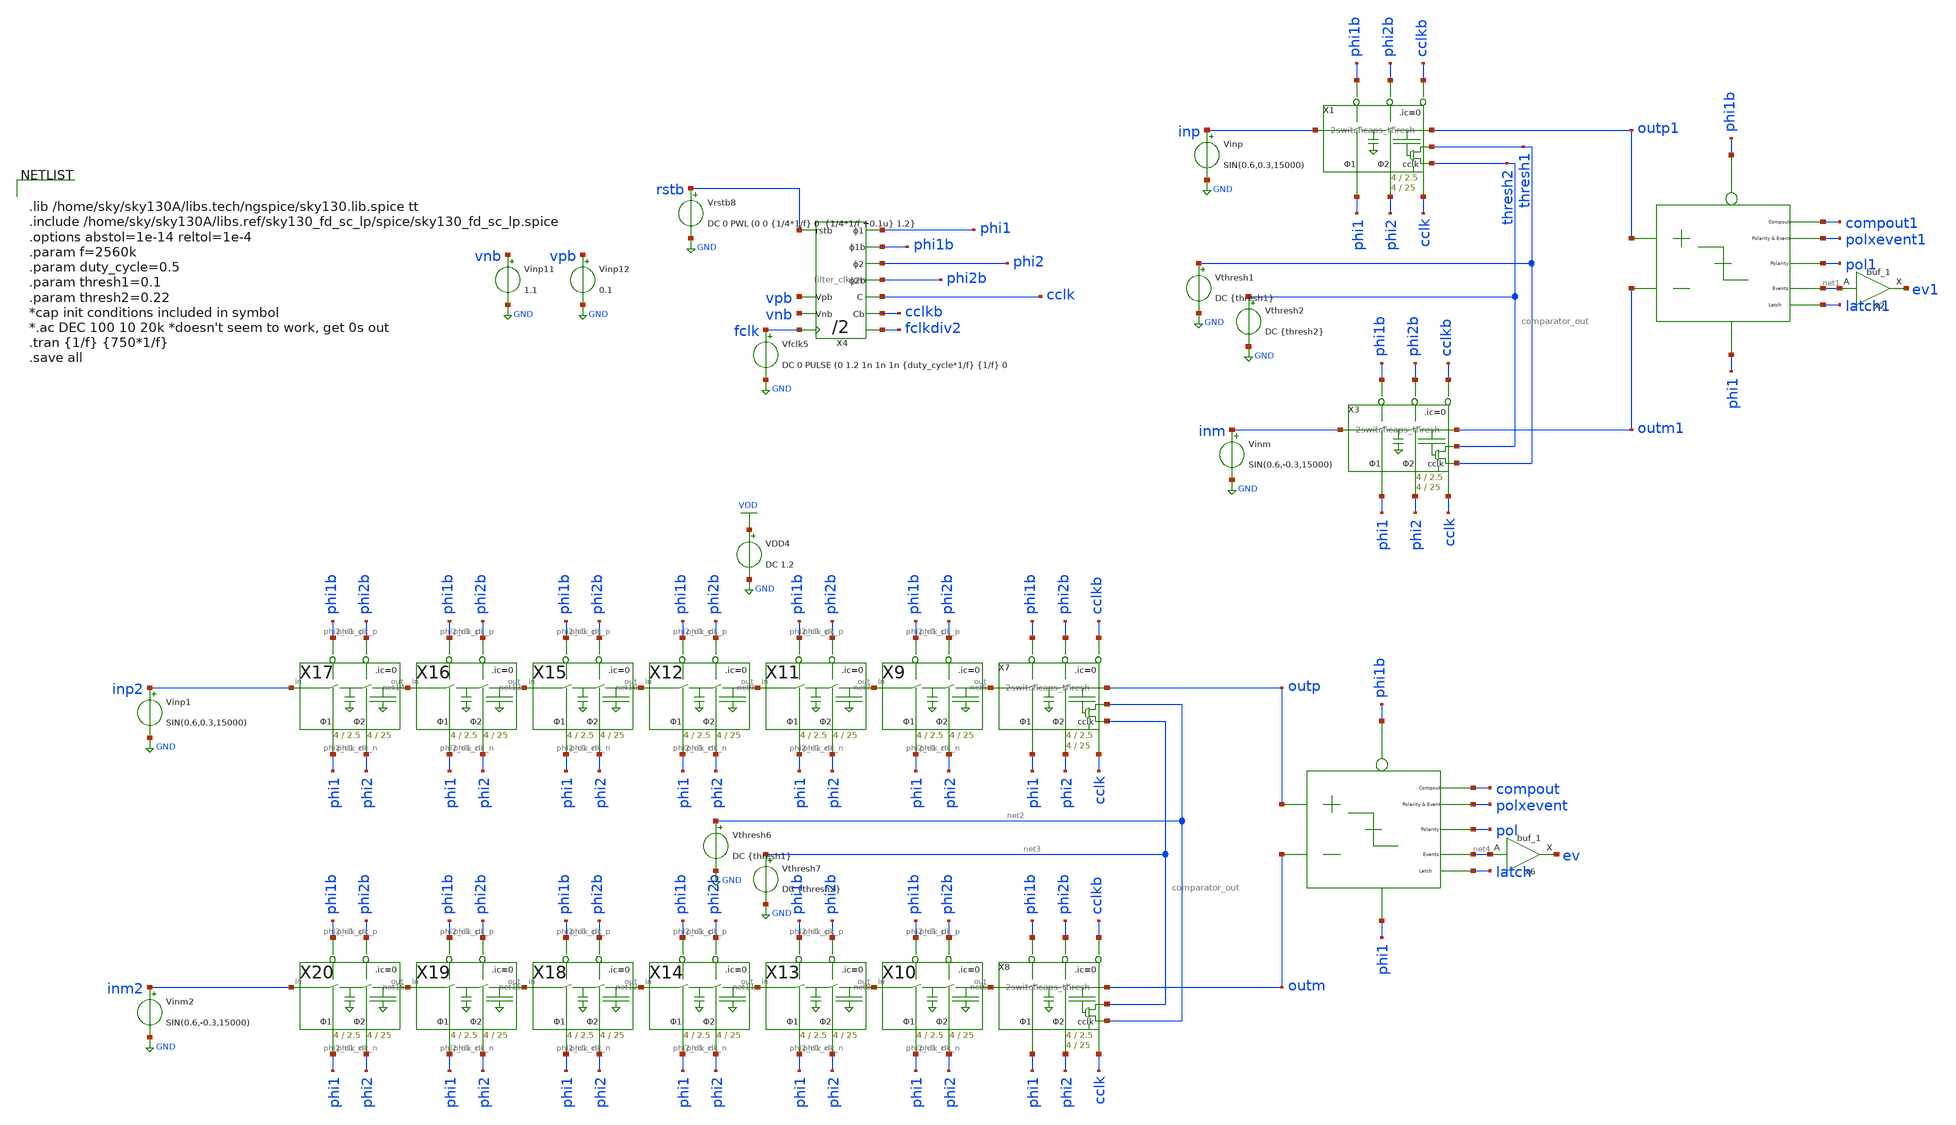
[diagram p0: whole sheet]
** sch_path: xschem/comparator/2switchcaps_thresh_diff_tb.sch
**.subckt 2switchcaps_thresh_diff_tb
Vinp inp GND SIN(0.6,0.3,15000)
Vthresh1 thresh1 GND DC {thresh1}
Vthresh2 thresh2 GND DC {thresh2}
Vinm inm GND SIN(0.6,-0.3,15000)
X1 inp outp1 phi2 phi1 phi1b phi2b thresh2 cclk thresh1 cclkb 2switchcaps_thresh Wcap1=4 Lcap1=2.5
+ Wcap2=4 Lcap2=25
X3 inm outm1 phi2 phi1 phi1b phi2b thresh1 cclk thresh2 cclkb 2switchcaps_thresh Wcap1=4 Lcap1=2.5
+ Wcap2=4 Lcap2=25
x1 phi1b phi1 outm1 outp1 net1 pol1 polxevent1 compout1 latch1 comparator_out
x2 net1 GND GND VDD VDD ev1 sky130_fd_sc_lp__buf_1
VDD4 VDD GND DC 1.2
Vfclk5 fclk GND DC 0 PULSE (0 1.2 1n 1n 1n {duty_cycle*1/f} {1/f} 0
X4 rstb fclk phi2b phi2 phi1b phi1 cclkb cclk fclkdiv2 vpb vnb filter_clkgen
Vthresh6 net2 GND DC {thresh1}
Vthresh7 net3 GND DC {thresh2}
Vrstb8 rstb GND DC 0 PWL (0 0 {1/4*1/f} 0 {1/4*1/f +0.1u} 1.2}
X7 net5 outp phi2 phi1 phi1b phi2b net3 cclk net2 cclkb 2switchcaps_thresh Wcap1=4 Lcap1=2.5 Wcap2=4 Lcap2=25
X8 net6 outm phi2 phi1 phi1b phi2b net2 cclk net3 cclkb 2switchcaps_thresh Wcap1=4 Lcap1=2.5 Wcap2=4 Lcap2=25
X9 net7 net5 phi2 phi1 phi1b phi2b 2switchcaps Wcap1=4 Lcap1=2.5 Wcap2=4 Lcap2=25
X10 net8 net6 phi2 phi1 phi1b phi2b 2switchcaps Wcap1=4 Lcap1=2.5 Wcap2=4 Lcap2=25
X11 net9 net7 phi2 phi1 phi1b phi2b 2switchcaps Wcap1=4 Lcap1=2.5 Wcap2=4 Lcap2=25
X12 net10 net9 phi2 phi1 phi1b phi2b 2switchcaps Wcap1=4 Lcap1=2.5 Wcap2=4 Lcap2=25
X13 net11 net8 phi2 phi1 phi1b phi2b 2switchcaps Wcap1=4 Lcap1=2.5 Wcap2=4 Lcap2=25
X14 net12 net11 phi2 phi1 phi1b phi2b 2switchcaps Wcap1=4 Lcap1=2.5 Wcap2=4 Lcap2=25
X15 net13 net10 phi2 phi1 phi1b phi2b 2switchcaps Wcap1=4 Lcap1=2.5 Wcap2=4 Lcap2=25
X16 net14 net13 phi2 phi1 phi1b phi2b 2switchcaps Wcap1=4 Lcap1=2.5 Wcap2=4 Lcap2=25
X17 inp2 net14 phi2 phi1 phi1b phi2b 2switchcaps Wcap1=4 Lcap1=2.5 Wcap2=4 Lcap2=25
X18 net15 net12 phi2 phi1 phi1b phi2b 2switchcaps Wcap1=4 Lcap1=2.5 Wcap2=4 Lcap2=25
X19 net16 net15 phi2 phi1 phi1b phi2b 2switchcaps Wcap1=4 Lcap1=2.5 Wcap2=4 Lcap2=25
X20 inm2 net16 phi2 phi1 phi1b phi2b 2switchcaps Wcap1=4 Lcap1=2.5 Wcap2=4 Lcap2=25
Vinp11 vnb GND 1.1
Vinp12 vpb GND 0.1
Vinp1 inp2 GND SIN(0.6,0.3,15000)
Vinm2 inm2 GND SIN(0.6,-0.3,15000)
x5 phi1b phi1 outm outp net4 pol polxevent compout latch comparator_out
x6 net4 GND GND VDD VDD ev sky130_fd_sc_lp__buf_1
**** begin user architecture code


.lib /home/sky/sky130A/libs.tech/ngspice/sky130.lib.spice tt
.include /home/sky/sky130A/libs.ref/sky130_fd_sc_lp/spice/sky130_fd_sc_lp.spice
.options abstol=1e-14 reltol=1e-4
.param f=2560k
.param duty_cycle=0.5
.param thresh1=0.1
.param thresh2=0.22
*cap init conditions included in symbol
*.ac DEC 100 10 20k *doesn't seem to work, get 0s out
.tran {1/f} {750*1/f}
.save all


**** end user architecture code
**.ends
.GLOBAL GND
.GLOBAL VDD
.end
